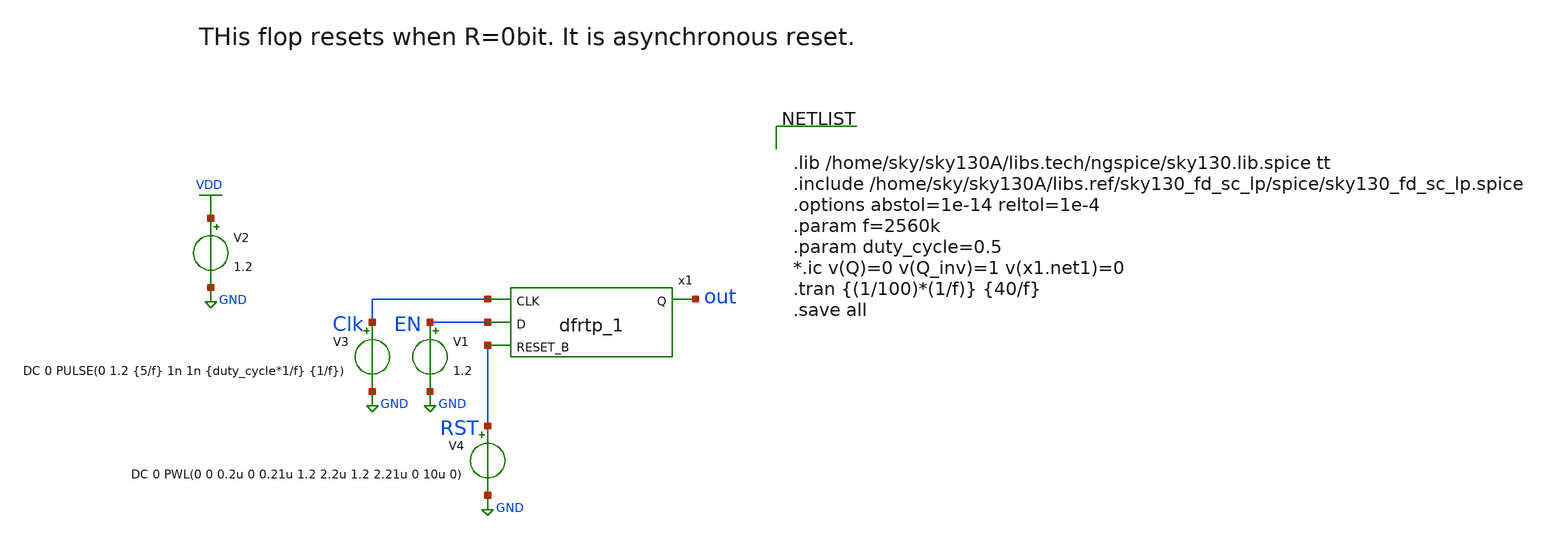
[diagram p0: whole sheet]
** sch_path: xschem/Asyn_rst_gray_counter/test_tb.sch
**.subckt test_tb
V3 Clk GND DC 0 PULSE(0 1.2 {5/f} 1n 1n {duty_cycle*1/f} {1/f})
V1 EN GND 1.2
V2 VDD GND 1.2
V4 RST GND DC 0 PWL(0 0 0.2u 0 0.21u 1.2 2.2u 1.2 2.21u 0 10u 0)
x1 Clk EN RST GND GND VDD VDD out sky130_fd_sc_lp__dfrtp_1
**** begin user architecture code


.lib /home/sky/sky130A/libs.tech/ngspice/sky130.lib.spice tt
.include /home/sky/sky130A/libs.ref/sky130_fd_sc_lp/spice/sky130_fd_sc_lp.spice
.options abstol=1e-14 reltol=1e-4
.param f=2560k
.param duty_cycle=0.5
*.ic v(Q)=0 v(Q_inv)=1 v(x1.net1)=0
.tran {(1/100)*(1/f)} {40/f}
.save all


**** end user architecture code
**.ends
.GLOBAL GND
.GLOBAL VDD
.end
